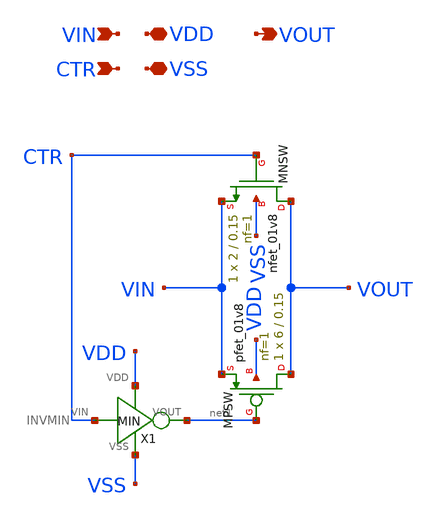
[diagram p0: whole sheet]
** sch_path: modules/PASSGATE/symbol/PASSGATE.sch
**.subckt PASSGATE VIN VDD VSS CTR VOUT
*.ipin VIN
*.iopin VDD
*.iopin VSS
*.ipin CTR
*.opin VOUT
XMNSW VOUT CTR VIN VSS sky130_fd_pr__nfet_01v8 L=0.15 W=2 nf=1 ad='int((nf+1)/2) * W/nf * 0.29' as='int((nf+2)/2) * W/nf * 0.29'
+ pd='2*int((nf+1)/2) * (W/nf + 0.29)' ps='2*int((nf+2)/2) * (W/nf + 0.29)' nrd='0.29 / W' nrs='0.29 / W'
+ sa=0 sb=0 sd=0 mult=1 m=1
XMPSW VOUT net1 VIN VDD sky130_fd_pr__pfet_01v8 L=0.15 W=6 nf=1 ad='int((nf+1)/2) * W/nf * 0.29' as='int((nf+2)/2) * W/nf * 0.29'
+ pd='2*int((nf+1)/2) * (W/nf + 0.29)' ps='2*int((nf+2)/2) * (W/nf + 0.29)' nrd='0.29 / W' nrs='0.29 / W'
+ sa=0 sb=0 sd=0 mult=1 m=1
X1 CTR net1 VDD VSS INVMIN
**.ends
.end
